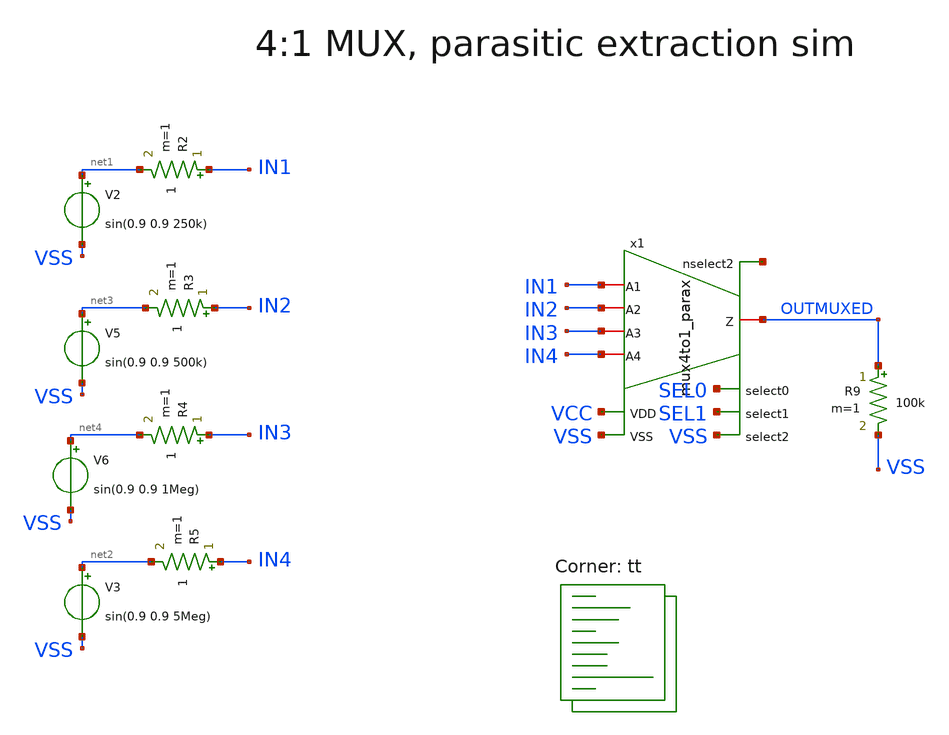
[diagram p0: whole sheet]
** sch_path: xschem/tb_4to1mux.sch
**.subckt tb_4to1mux
V2 net1 VSS sin(0.9 0.9 250k)
V3 net2 VSS sin(0.9 0.9 5Meg)
V5 net3 VSS sin(0.9 0.9 500k)
V6 net4 VSS sin(0.9 0.9 1Meg)
R2 IN1 net1 1 m=1
R3 IN2 net3 1 m=1
R4 IN3 net4 1 m=1
R5 IN4 net2 1 m=1
R9 OUTMUXED VSS 100k m=1
x1 SEL0 SEL1 VSS IN1 IN2 IN3 IN4 OUTMUXED net5 VCC VSS mux4to1_parax
**** begin user architecture code
.lib $::SKYWATER_MODELS/sky130.lib.spice tt
**** end user architecture code
**.ends

* expanding   symbol:  /home/ttuser/vmswap/analogmuxkit/xschem/mux4to1_parax.sym # of pins=11
** sym_path: xschem/mux4to1.sym
.include [file normalize extracted/mux4to1_parax.spice]
**** begin user architecture code


* ngspice commands
* .options savecurrents
.param VCC = 1.8
.param SRCRES = 1k
.include stimuli_tb_4to1mux.cir
.control
save all
op
write tb_4to1mux.raw
set appendwrite
tran 50n 70u
write tb_4to1mux.raw
quit 0
.endc



**** end user architecture code
.end
